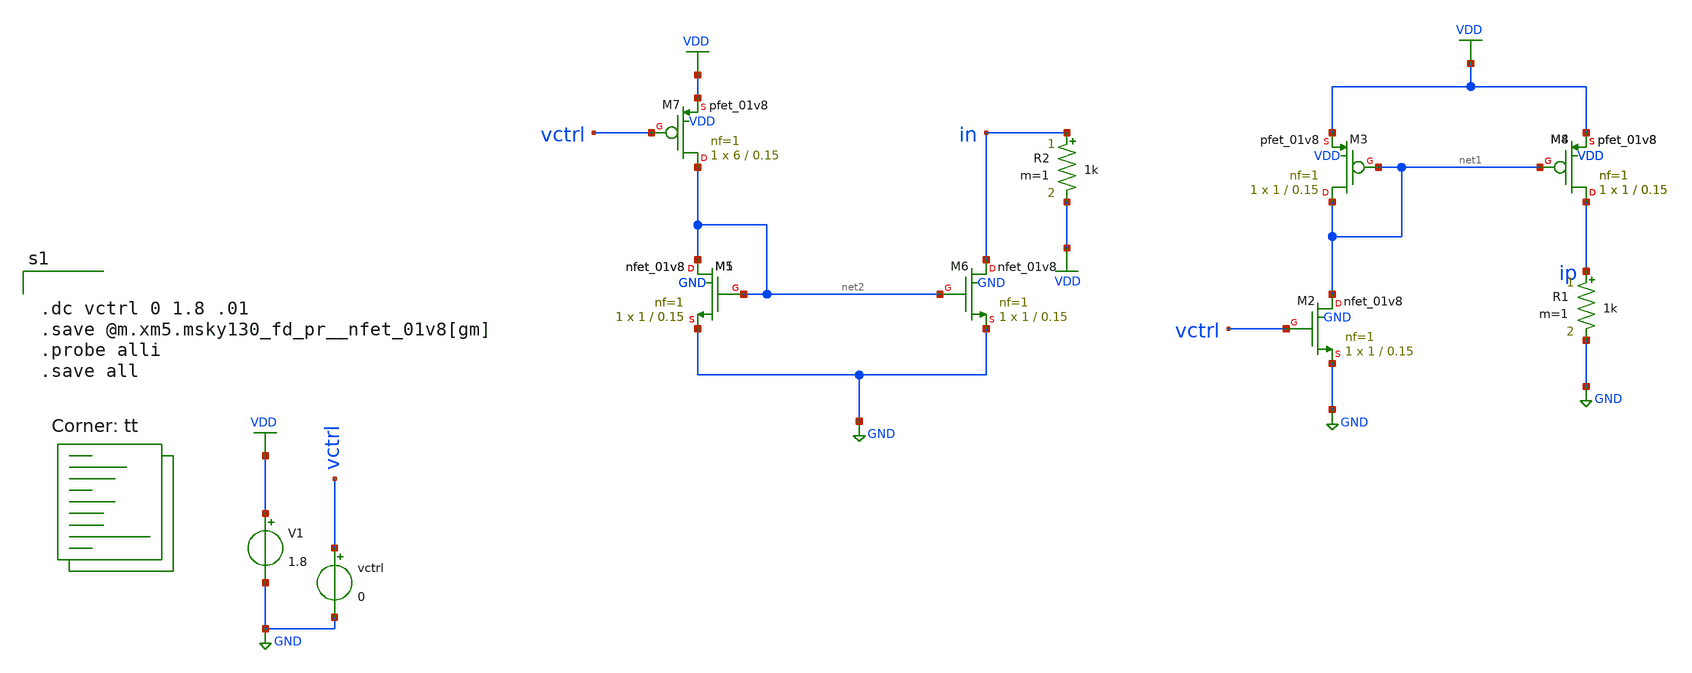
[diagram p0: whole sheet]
** sch_path: pll/ring_vco_lib/QRO_TB/xschem/current_mirror_test.sch
**.subckt current_mirror_test
XM3 net1 net1 VDD VDD sky130_fd_pr__pfet_01v8 L=0.15 W=1 nf=1 ad='int((nf+1)/2) * W/nf * 0.29' as='int((nf+2)/2) * W/nf * 0.29'
+ pd='2*int((nf+1)/2) * (W/nf + 0.29)' ps='2*int((nf+2)/2) * (W/nf + 0.29)' nrd='0.29 / W' nrs='0.29 / W'
+ sa=0 sb=0 sd=0 mult=1 m=1
XM4 ip net1 VDD VDD sky130_fd_pr__pfet_01v8 L=0.15 W=1 nf=1 ad='int((nf+1)/2) * W/nf * 0.29' as='int((nf+2)/2) * W/nf * 0.29'
+ pd='2*int((nf+1)/2) * (W/nf + 0.29)' ps='2*int((nf+2)/2) * (W/nf + 0.29)' nrd='0.29 / W' nrs='0.29 / W'
+ sa=0 sb=0 sd=0 mult=1 m=1
XM5 net2 net2 GND GND sky130_fd_pr__nfet_01v8 L=0.15 W=1 nf=1 ad='int((nf+1)/2) * W/nf * 0.29' as='int((nf+2)/2) * W/nf * 0.29'
+ pd='2*int((nf+1)/2) * (W/nf + 0.29)' ps='2*int((nf+2)/2) * (W/nf + 0.29)' nrd='0.29 / W' nrs='0.29 / W'
+ sa=0 sb=0 sd=0 mult=1 m=1
XM6 in net2 GND GND sky130_fd_pr__nfet_01v8 L=0.15 W=1 nf=1 ad='int((nf+1)/2) * W/nf * 0.29' as='int((nf+2)/2) * W/nf * 0.29'
+ pd='2*int((nf+1)/2) * (W/nf + 0.29)' ps='2*int((nf+2)/2) * (W/nf + 0.29)' nrd='0.29 / W' nrs='0.29 / W'
+ sa=0 sb=0 sd=0 mult=1 m=1
V1 VDD GND 1.8
vctrl vctrl GND 0
R1 ip GND 1k m=1
R2 in VDD 1k m=1
XM1 net2 net2 GND GND sky130_fd_pr__nfet_01v8 L=0.15 W=1 nf=1 ad='int((nf+1)/2) * W/nf * 0.29' as='int((nf+2)/2) * W/nf * 0.29'
+ pd='2*int((nf+1)/2) * (W/nf + 0.29)' ps='2*int((nf+2)/2) * (W/nf + 0.29)' nrd='0.29 / W' nrs='0.29 / W'
+ sa=0 sb=0 sd=0 mult=1 m=1
XM2 net1 vctrl GND GND sky130_fd_pr__nfet_01v8 L=0.15 W=1 nf=1 ad='int((nf+1)/2) * W/nf * 0.29' as='int((nf+2)/2) * W/nf * 0.29'
+ pd='2*int((nf+1)/2) * (W/nf + 0.29)' ps='2*int((nf+2)/2) * (W/nf + 0.29)' nrd='0.29 / W' nrs='0.29 / W'
+ sa=0 sb=0 sd=0 mult=1 m=1
XM7 net2 vctrl VDD VDD sky130_fd_pr__pfet_01v8 L=0.15 W=6 nf=1 ad='int((nf+1)/2) * W/nf * 0.29' as='int((nf+2)/2) * W/nf * 0.29'
+ pd='2*int((nf+1)/2) * (W/nf + 0.29)' ps='2*int((nf+2)/2) * (W/nf + 0.29)' nrd='0.29 / W' nrs='0.29 / W'
+ sa=0 sb=0 sd=0 mult=1 m=1
XM8 ip net1 VDD VDD sky130_fd_pr__pfet_01v8 L=0.15 W=1 nf=1 ad='int((nf+1)/2) * W/nf * 0.29' as='int((nf+2)/2) * W/nf * 0.29'
+ pd='2*int((nf+1)/2) * (W/nf + 0.29)' ps='2*int((nf+2)/2) * (W/nf + 0.29)' nrd='0.29 / W' nrs='0.29 / W'
+ sa=0 sb=0 sd=0 mult=1 m=1
**** begin user architecture code


.dc vctrl 0 1.8 .01
.save @m.xm5.msky130_fd_pr__nfet_01v8[gm]
.probe alli
.save all

.lib $::SKYWATER_MODELS/sky130.lib.spice tt
**** end user architecture code
**.ends
.GLOBAL GND
.GLOBAL VDD
.end
